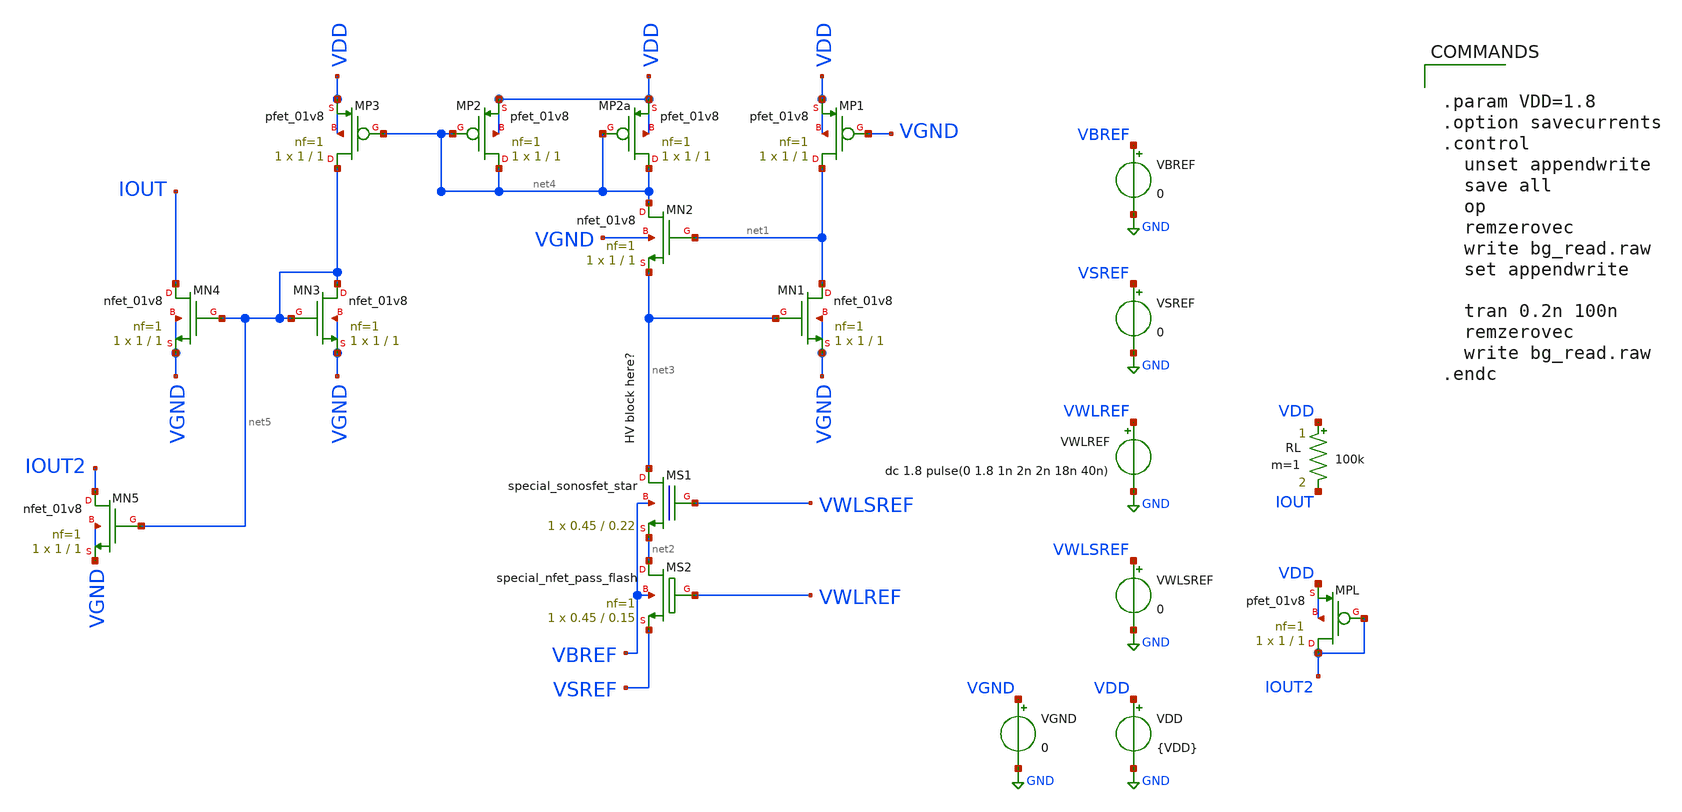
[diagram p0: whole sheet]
** sch_path: read/bg_read.sch
**.subckt bg_read
XMN1 net1 net3 VGND VGND sky130_fd_pr__nfet_01v8 L=1 W=1 nf=1 ad='int((nf+1)/2) * W/nf * 0.29' as='int((nf+2)/2) * W/nf * 0.29'
+ pd='2*int((nf+1)/2) * (W/nf + 0.29)' ps='2*int((nf+2)/2) * (W/nf + 0.29)' nrd='0.29 / W' nrs='0.29 / W'
+ sa=0 sb=0 sd=0 mult=1 m=1
XMP1 net1 VGND VDD VDD sky130_fd_pr__pfet_01v8 L=1 W=1 nf=1 ad='int((nf+1)/2) * W/nf * 0.29' as='int((nf+2)/2) * W/nf * 0.29'
+ pd='2*int((nf+1)/2) * (W/nf + 0.29)' ps='2*int((nf+2)/2) * (W/nf + 0.29)' nrd='0.29 / W' nrs='0.29 / W'
+ sa=0 sb=0 sd=0 mult=1 m=1
XMN2 net4 net1 net3 VGND sky130_fd_pr__nfet_01v8 L=1 W=1 nf=1 ad='int((nf+1)/2) * W/nf * 0.29' as='int((nf+2)/2) * W/nf * 0.29'
+ pd='2*int((nf+1)/2) * (W/nf + 0.29)' ps='2*int((nf+2)/2) * (W/nf + 0.29)' nrd='0.29 / W' nrs='0.29 / W'
+ sa=0 sb=0 sd=0 mult=1 m=1
XMS1 net3 VWLSREF net2 VBREF sky130_fd_bs_flash__special_sonosfet_star L=0.22 W=0.45 nf=1 ad='1 * W * 0.29'
+ as='1 * W * 0.29' pd='2 * (W + 0.29)' ps='2 * (W + 0.29)' nrd='0.29 / W' nrs='0.29 / W' sa=0 sb=0 sd=0
+ mult=1 m=1
XMS2 net2 VWLREF VSREF VBREF sky130_fd_pr__special_nfet_pass_flash L=0.15 W=0.45 nf=1 ad='1 * W * 0.29'
+ as='1 * W * 0.29' pd='2 * (W + 0.29)' ps='2 * (W + 0.29)' nrd='0.29 / W' nrs='0.29 / W' sa=0 sb=0 sd=0
+ mult=1 m=1
XMP2a net4 net4 VDD VDD sky130_fd_pr__pfet_01v8 L=1 W=1 nf=1 ad='int((nf+1)/2) * W/nf * 0.29' as='int((nf+2)/2) * W/nf * 0.29'
+ pd='2*int((nf+1)/2) * (W/nf + 0.29)' ps='2*int((nf+2)/2) * (W/nf + 0.29)' nrd='0.29 / W' nrs='0.29 / W'
+ sa=0 sb=0 sd=0 mult=1 m=1
XMP3 net5 net4 VDD VDD sky130_fd_pr__pfet_01v8 L=1 W=1 nf=1 ad='int((nf+1)/2) * W/nf * 0.29' as='int((nf+2)/2) * W/nf * 0.29'
+ pd='2*int((nf+1)/2) * (W/nf + 0.29)' ps='2*int((nf+2)/2) * (W/nf + 0.29)' nrd='0.29 / W' nrs='0.29 / W'
+ sa=0 sb=0 sd=0 mult=1 m=1
XMN3 net5 net5 VGND VGND sky130_fd_pr__nfet_01v8 L=1 W=1 nf=1 ad='int((nf+1)/2) * W/nf * 0.29' as='int((nf+2)/2) * W/nf * 0.29'
+ pd='2*int((nf+1)/2) * (W/nf + 0.29)' ps='2*int((nf+2)/2) * (W/nf + 0.29)' nrd='0.29 / W' nrs='0.29 / W'
+ sa=0 sb=0 sd=0 mult=1 m=1
XMN4 IOUT net5 VGND VGND sky130_fd_pr__nfet_01v8 L=1 W=1 nf=1 ad='int((nf+1)/2) * W/nf * 0.29' as='int((nf+2)/2) * W/nf * 0.29'
+ pd='2*int((nf+1)/2) * (W/nf + 0.29)' ps='2*int((nf+2)/2) * (W/nf + 0.29)' nrd='0.29 / W' nrs='0.29 / W'
+ sa=0 sb=0 sd=0 mult=1 m=1
XMP2 net4 net4 VDD VDD sky130_fd_pr__pfet_01v8 L=1 W=1 nf=1 ad='int((nf+1)/2) * W/nf * 0.29' as='int((nf+2)/2) * W/nf * 0.29'
+ pd='2*int((nf+1)/2) * (W/nf + 0.29)' ps='2*int((nf+2)/2) * (W/nf + 0.29)' nrd='0.29 / W' nrs='0.29 / W'
+ sa=0 sb=0 sd=0 mult=1 m=1
VDD VDD GND {VDD}
VGND VGND GND 0
VWLSREF VWLSREF GND 0
VWLREF VWLREF GND dc 1.8 pulse(0 1.8 1n 2n 2n 18n 40n)
RL VDD IOUT 100k m=1
VSREF VSREF GND 0
VBREF VBREF GND 0
XMN5 IOUT2 net5 VGND VGND sky130_fd_pr__nfet_01v8 L=1 W=1 nf=1 ad='int((nf+1)/2) * W/nf * 0.29' as='int((nf+2)/2) * W/nf * 0.29'
+ pd='2*int((nf+1)/2) * (W/nf + 0.29)' ps='2*int((nf+2)/2) * (W/nf + 0.29)' nrd='0.29 / W' nrs='0.29 / W'
+ sa=0 sb=0 sd=0 mult=1 m=1
XMPL IOUT2 IOUT2 VDD VDD sky130_fd_pr__pfet_01v8 L=1 W=1 nf=1 ad='int((nf+1)/2) * W/nf * 0.29' as='int((nf+2)/2) * W/nf * 0.29'
+ pd='2*int((nf+1)/2) * (W/nf + 0.29)' ps='2*int((nf+2)/2) * (W/nf + 0.29)' nrd='0.29 / W' nrs='0.29 / W'
+ sa=0 sb=0 sd=0 mult=1 m=1
**** begin user architecture code

** opencircuitdesign pdks install
.lib $::SKYWATER_MODELS/sky130.lib.spice tt
.include $::SKYWATER_MODELS/sonos_e/begin_of_life.spice
.include $::SKYWATER_MODELS/sonos_e/begin_of_life.pm3.spice
.include $::SKYWATER_MODELS/sonos_p/begin_of_life.spice
.include $::SKYWATER_MODELS/sonos_p/begin_of_life.pm3.spice



.param VDD=1.8
.option savecurrents
.control
  unset appendwrite
  save all
  op
  remzerovec
  write bg_read.raw
  set appendwrite

  tran 0.2n 100n
  remzerovec
  write bg_read.raw
.endc


**** end user architecture code
**.ends
.GLOBAL GND
.end
